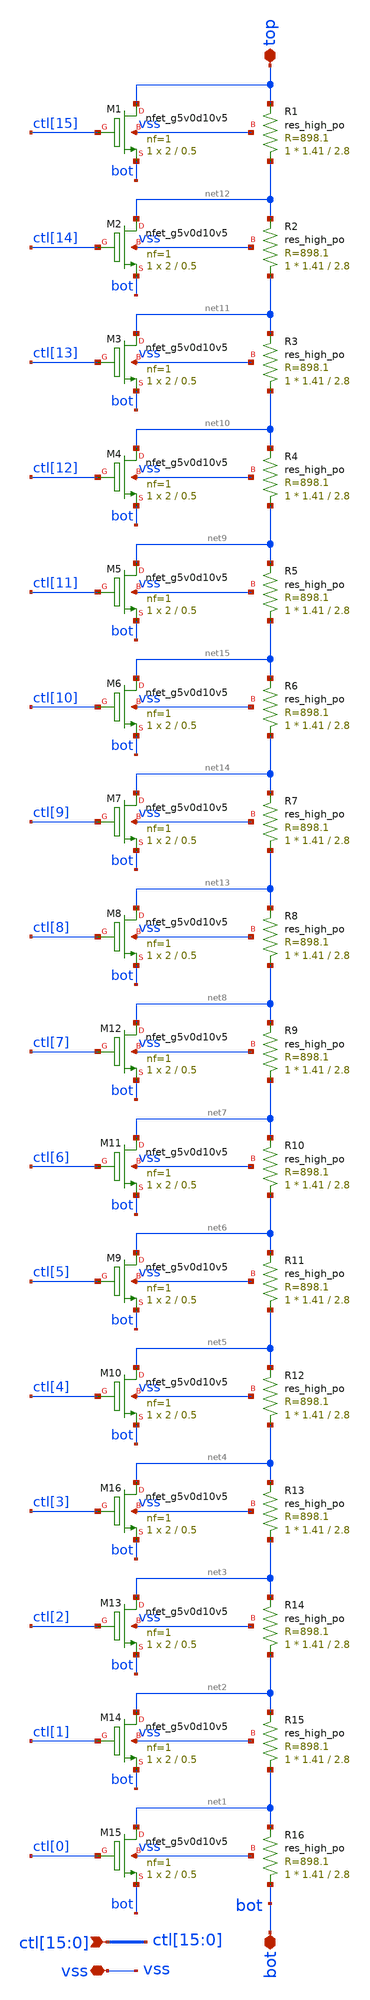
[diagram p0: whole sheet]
** sch_path: schematic/bg_trim.sch
**.subckt bg_trim vss bot top
*+ ctl[15],ctl[14],ctl[13],ctl[12],ctl[11],ctl[10],ctl[9],ctl[8],ctl[7],ctl[6],ctl[5],ctl[4],ctl[3],ctl[2],ctl[1],ctl[0]
*.iopin vss
*.iopin bot
*.iopin top
*.ipin
*+ ctl[15],ctl[14],ctl[13],ctl[12],ctl[11],ctl[10],ctl[9],ctl[8],ctl[7],ctl[6],ctl[5],ctl[4],ctl[3],ctl[2],ctl[1],ctl[0]
XM1 top ctl[15] bot vss sky130_fd_pr__nfet_g5v0d10v5 L=0.5 W=2 nf=1 ad='int((nf+1)/2) * W/nf * 0.29'
+ as='int((nf+2)/2) * W/nf * 0.29' pd='2*int((nf+1)/2) * (W/nf + 0.29)' ps='2*int((nf+2)/2) * (W/nf + 0.29)'
+ nrd='0.29 / W' nrs='0.29 / W' sa=0 sb=0 sd=0 mult=1 m=1
XM2 net12 ctl[14] bot vss sky130_fd_pr__nfet_g5v0d10v5 L=0.5 W=2 nf=1 ad='int((nf+1)/2) * W/nf * 0.29'
+ as='int((nf+2)/2) * W/nf * 0.29' pd='2*int((nf+1)/2) * (W/nf + 0.29)' ps='2*int((nf+2)/2) * (W/nf + 0.29)'
+ nrd='0.29 / W' nrs='0.29 / W' sa=0 sb=0 sd=0 mult=1 m=1
XM3 net11 ctl[13] bot vss sky130_fd_pr__nfet_g5v0d10v5 L=0.5 W=2 nf=1 ad='int((nf+1)/2) * W/nf * 0.29'
+ as='int((nf+2)/2) * W/nf * 0.29' pd='2*int((nf+1)/2) * (W/nf + 0.29)' ps='2*int((nf+2)/2) * (W/nf + 0.29)'
+ nrd='0.29 / W' nrs='0.29 / W' sa=0 sb=0 sd=0 mult=1 m=1
XM4 net10 ctl[12] bot vss sky130_fd_pr__nfet_g5v0d10v5 L=0.5 W=2 nf=1 ad='int((nf+1)/2) * W/nf * 0.29'
+ as='int((nf+2)/2) * W/nf * 0.29' pd='2*int((nf+1)/2) * (W/nf + 0.29)' ps='2*int((nf+2)/2) * (W/nf + 0.29)'
+ nrd='0.29 / W' nrs='0.29 / W' sa=0 sb=0 sd=0 mult=1 m=1
XM5 net9 ctl[11] bot vss sky130_fd_pr__nfet_g5v0d10v5 L=0.5 W=2 nf=1 ad='int((nf+1)/2) * W/nf * 0.29'
+ as='int((nf+2)/2) * W/nf * 0.29' pd='2*int((nf+1)/2) * (W/nf + 0.29)' ps='2*int((nf+2)/2) * (W/nf + 0.29)'
+ nrd='0.29 / W' nrs='0.29 / W' sa=0 sb=0 sd=0 mult=1 m=1
XM6 net15 ctl[10] bot vss sky130_fd_pr__nfet_g5v0d10v5 L=0.5 W=2 nf=1 ad='int((nf+1)/2) * W/nf * 0.29'
+ as='int((nf+2)/2) * W/nf * 0.29' pd='2*int((nf+1)/2) * (W/nf + 0.29)' ps='2*int((nf+2)/2) * (W/nf + 0.29)'
+ nrd='0.29 / W' nrs='0.29 / W' sa=0 sb=0 sd=0 mult=1 m=1
XM7 net14 ctl[9] bot vss sky130_fd_pr__nfet_g5v0d10v5 L=0.5 W=2 nf=1 ad='int((nf+1)/2) * W/nf * 0.29'
+ as='int((nf+2)/2) * W/nf * 0.29' pd='2*int((nf+1)/2) * (W/nf + 0.29)' ps='2*int((nf+2)/2) * (W/nf + 0.29)'
+ nrd='0.29 / W' nrs='0.29 / W' sa=0 sb=0 sd=0 mult=1 m=1
XM8 net13 ctl[8] bot vss sky130_fd_pr__nfet_g5v0d10v5 L=0.5 W=2 nf=1 ad='int((nf+1)/2) * W/nf * 0.29'
+ as='int((nf+2)/2) * W/nf * 0.29' pd='2*int((nf+1)/2) * (W/nf + 0.29)' ps='2*int((nf+2)/2) * (W/nf + 0.29)'
+ nrd='0.29 / W' nrs='0.29 / W' sa=0 sb=0 sd=0 mult=1 m=1
XM9 net6 ctl[5] bot vss sky130_fd_pr__nfet_g5v0d10v5 L=0.5 W=2 nf=1 ad='int((nf+1)/2) * W/nf * 0.29'
+ as='int((nf+2)/2) * W/nf * 0.29' pd='2*int((nf+1)/2) * (W/nf + 0.29)' ps='2*int((nf+2)/2) * (W/nf + 0.29)'
+ nrd='0.29 / W' nrs='0.29 / W' sa=0 sb=0 sd=0 mult=1 m=1
XM10 net5 ctl[4] bot vss sky130_fd_pr__nfet_g5v0d10v5 L=0.5 W=2 nf=1 ad='int((nf+1)/2) * W/nf * 0.29'
+ as='int((nf+2)/2) * W/nf * 0.29' pd='2*int((nf+1)/2) * (W/nf + 0.29)' ps='2*int((nf+2)/2) * (W/nf + 0.29)'
+ nrd='0.29 / W' nrs='0.29 / W' sa=0 sb=0 sd=0 mult=1 m=1
XM11 net7 ctl[6] bot vss sky130_fd_pr__nfet_g5v0d10v5 L=0.5 W=2 nf=1 ad='int((nf+1)/2) * W/nf * 0.29'
+ as='int((nf+2)/2) * W/nf * 0.29' pd='2*int((nf+1)/2) * (W/nf + 0.29)' ps='2*int((nf+2)/2) * (W/nf + 0.29)'
+ nrd='0.29 / W' nrs='0.29 / W' sa=0 sb=0 sd=0 mult=1 m=1
XM12 net8 ctl[7] bot vss sky130_fd_pr__nfet_g5v0d10v5 L=0.5 W=2 nf=1 ad='int((nf+1)/2) * W/nf * 0.29'
+ as='int((nf+2)/2) * W/nf * 0.29' pd='2*int((nf+1)/2) * (W/nf + 0.29)' ps='2*int((nf+2)/2) * (W/nf + 0.29)'
+ nrd='0.29 / W' nrs='0.29 / W' sa=0 sb=0 sd=0 mult=1 m=1
XM13 net3 ctl[2] bot vss sky130_fd_pr__nfet_g5v0d10v5 L=0.5 W=2 nf=1 ad='int((nf+1)/2) * W/nf * 0.29'
+ as='int((nf+2)/2) * W/nf * 0.29' pd='2*int((nf+1)/2) * (W/nf + 0.29)' ps='2*int((nf+2)/2) * (W/nf + 0.29)'
+ nrd='0.29 / W' nrs='0.29 / W' sa=0 sb=0 sd=0 mult=1 m=1
XM14 net2 ctl[1] bot vss sky130_fd_pr__nfet_g5v0d10v5 L=0.5 W=2 nf=1 ad='int((nf+1)/2) * W/nf * 0.29'
+ as='int((nf+2)/2) * W/nf * 0.29' pd='2*int((nf+1)/2) * (W/nf + 0.29)' ps='2*int((nf+2)/2) * (W/nf + 0.29)'
+ nrd='0.29 / W' nrs='0.29 / W' sa=0 sb=0 sd=0 mult=1 m=1
XM15 net1 ctl[0] bot vss sky130_fd_pr__nfet_g5v0d10v5 L=0.5 W=2 nf=1 ad='int((nf+1)/2) * W/nf * 0.29'
+ as='int((nf+2)/2) * W/nf * 0.29' pd='2*int((nf+1)/2) * (W/nf + 0.29)' ps='2*int((nf+2)/2) * (W/nf + 0.29)'
+ nrd='0.29 / W' nrs='0.29 / W' sa=0 sb=0 sd=0 mult=1 m=1
XM16 net4 ctl[3] bot vss sky130_fd_pr__nfet_g5v0d10v5 L=0.5 W=2 nf=1 ad='int((nf+1)/2) * W/nf * 0.29'
+ as='int((nf+2)/2) * W/nf * 0.29' pd='2*int((nf+1)/2) * (W/nf + 0.29)' ps='2*int((nf+2)/2) * (W/nf + 0.29)'
+ nrd='0.29 / W' nrs='0.29 / W' sa=0 sb=0 sd=0 mult=1 m=1
XR1 net12 top vss sky130_fd_pr__res_high_po W=1.41 L=2.8 mult=1 m=1
XR2 net11 net12 vss sky130_fd_pr__res_high_po W=1.41 L=2.8 mult=1 m=1
XR3 net10 net11 vss sky130_fd_pr__res_high_po W=1.41 L=2.8 mult=1 m=1
XR4 net9 net10 vss sky130_fd_pr__res_high_po W=1.41 L=2.8 mult=1 m=1
XR5 net15 net9 vss sky130_fd_pr__res_high_po W=1.41 L=2.8 mult=1 m=1
XR6 net14 net15 vss sky130_fd_pr__res_high_po W=1.41 L=2.8 mult=1 m=1
XR7 net13 net14 vss sky130_fd_pr__res_high_po W=1.41 L=2.8 mult=1 m=1
XR8 net8 net13 vss sky130_fd_pr__res_high_po W=1.41 L=2.8 mult=1 m=1
XR9 net7 net8 vss sky130_fd_pr__res_high_po W=1.41 L=2.8 mult=1 m=1
XR10 net6 net7 vss sky130_fd_pr__res_high_po W=1.41 L=2.8 mult=1 m=1
XR11 net5 net6 vss sky130_fd_pr__res_high_po W=1.41 L=2.8 mult=1 m=1
XR12 net4 net5 vss sky130_fd_pr__res_high_po W=1.41 L=2.8 mult=1 m=1
XR13 net3 net4 vss sky130_fd_pr__res_high_po W=1.41 L=2.8 mult=1 m=1
XR14 net2 net3 vss sky130_fd_pr__res_high_po W=1.41 L=2.8 mult=1 m=1
XR15 net1 net2 vss sky130_fd_pr__res_high_po W=1.41 L=2.8 mult=1 m=1
XR16 bot net1 vss sky130_fd_pr__res_high_po W=1.41 L=2.8 mult=1 m=1
**.ends
.end
